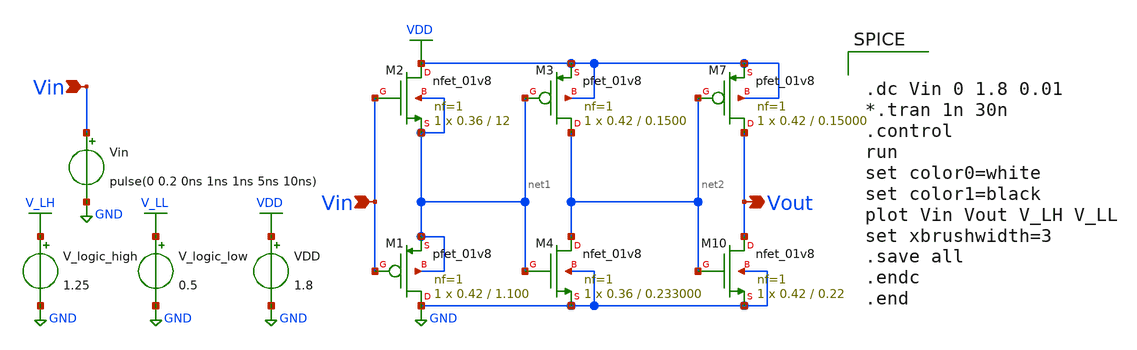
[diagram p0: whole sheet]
** sch_path: xschem/Vth_sch/th01.sch
**.subckt th01 Vin Vin Vout
*.ipin Vin
*.ipin Vin
*.opin Vout
VDD VDD GND 1.8
Vin Vin GND pulse(0 0.2 0ns 1ns 1ns 5ns 10ns)
V_logic_high V_LH GND 1.25
V_logic_low V_LL GND 0.5
XM1 GND Vin net1 net1 sky130_fd_pr__pfet_01v8 L=1.100 W=0.42 nf=1 ad='int((nf+1)/2) * W/nf * 0.29' as='int((nf+2)/2) * W/nf * 0.29'
+ pd='2*int((nf+1)/2) * (W/nf + 0.29)' ps='2*int((nf+2)/2) * (W/nf + 0.29)' nrd='0.29 / W' nrs='0.29 / W'
+ sa=0 sb=0 sd=0 mult=1 m=1
XM2 VDD Vin net1 net1 sky130_fd_pr__nfet_01v8 L=12 W=0.36 nf=1 ad='int((nf+1)/2) * W/nf * 0.29' as='int((nf+2)/2) * W/nf * 0.29'
+ pd='2*int((nf+1)/2) * (W/nf + 0.29)' ps='2*int((nf+2)/2) * (W/nf + 0.29)' nrd='0.29 / W' nrs='0.29 / W'
+ sa=0 sb=0 sd=0 mult=1 m=1
XM7 Vout net2 VDD VDD sky130_fd_pr__pfet_01v8 L=0.15000 W=0.42 nf=1 ad='int((nf+1)/2) * W/nf * 0.29'
+ as='int((nf+2)/2) * W/nf * 0.29' pd='2*int((nf+1)/2) * (W/nf + 0.29)' ps='2*int((nf+2)/2) * (W/nf + 0.29)'
+ nrd='0.29 / W' nrs='0.29 / W' sa=0 sb=0 sd=0 mult=1 m=1
XM10 Vout net2 GND GND sky130_fd_pr__nfet_01v8 L=0.22 W=0.42 nf=1 ad='int((nf+1)/2) * W/nf * 0.29' as='int((nf+2)/2) * W/nf * 0.29'
+ pd='2*int((nf+1)/2) * (W/nf + 0.29)' ps='2*int((nf+2)/2) * (W/nf + 0.29)' nrd='0.29 / W' nrs='0.29 / W'
+ sa=0 sb=0 sd=0 mult=1 m=1
XM3 net2 net1 VDD VDD sky130_fd_pr__pfet_01v8 L=0.1500 W=0.42 nf=1 ad='int((nf+1)/2) * W/nf * 0.29' as='int((nf+2)/2) * W/nf * 0.29'
+ pd='2*int((nf+1)/2) * (W/nf + 0.29)' ps='2*int((nf+2)/2) * (W/nf + 0.29)' nrd='0.29 / W' nrs='0.29 / W'
+ sa=0 sb=0 sd=0 mult=1 m=1
XM4 net2 net1 GND GND sky130_fd_pr__nfet_01v8 L=0.233000 W=0.36 nf=1 ad='int((nf+1)/2) * W/nf * 0.29'
+ as='int((nf+2)/2) * W/nf * 0.29' pd='2*int((nf+1)/2) * (W/nf + 0.29)' ps='2*int((nf+2)/2) * (W/nf + 0.29)'
+ nrd='0.29 / W' nrs='0.29 / W' sa=0 sb=0 sd=0 mult=1 m=1
**** begin user architecture code


.lib /usr/local/share/pdk/sky130A/libs.tech/ngspice/sky130.lib.spice tt

.save all





.dc Vin 0 1.8 0.01
*.tran 1n 30n
.control
run
set color0=white
set color1=black
plot Vin Vout V_LH V_LL
set xbrushwidth=3
.save all
.endc
.end


**** end user architecture code
**.ends
.GLOBAL VDD
.GLOBAL GND
.GLOBAL V_LH
.GLOBAL V_LL
.end
